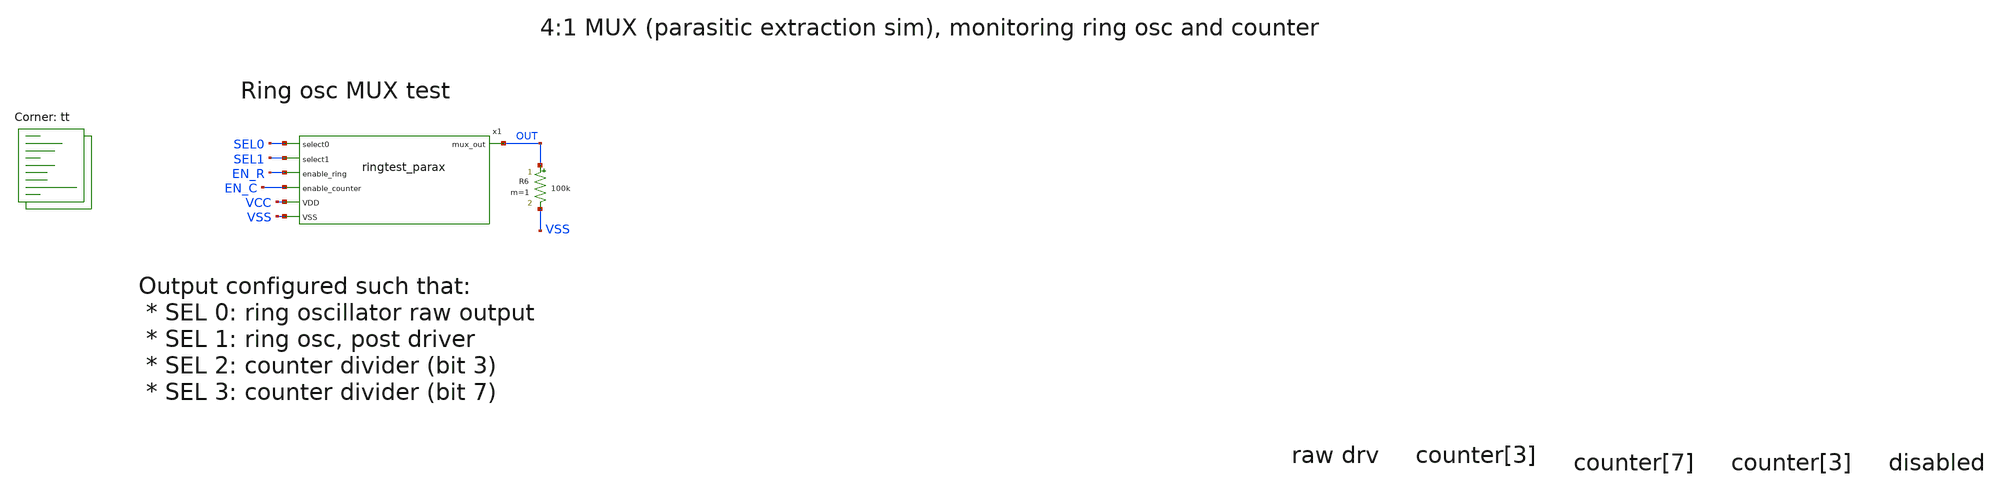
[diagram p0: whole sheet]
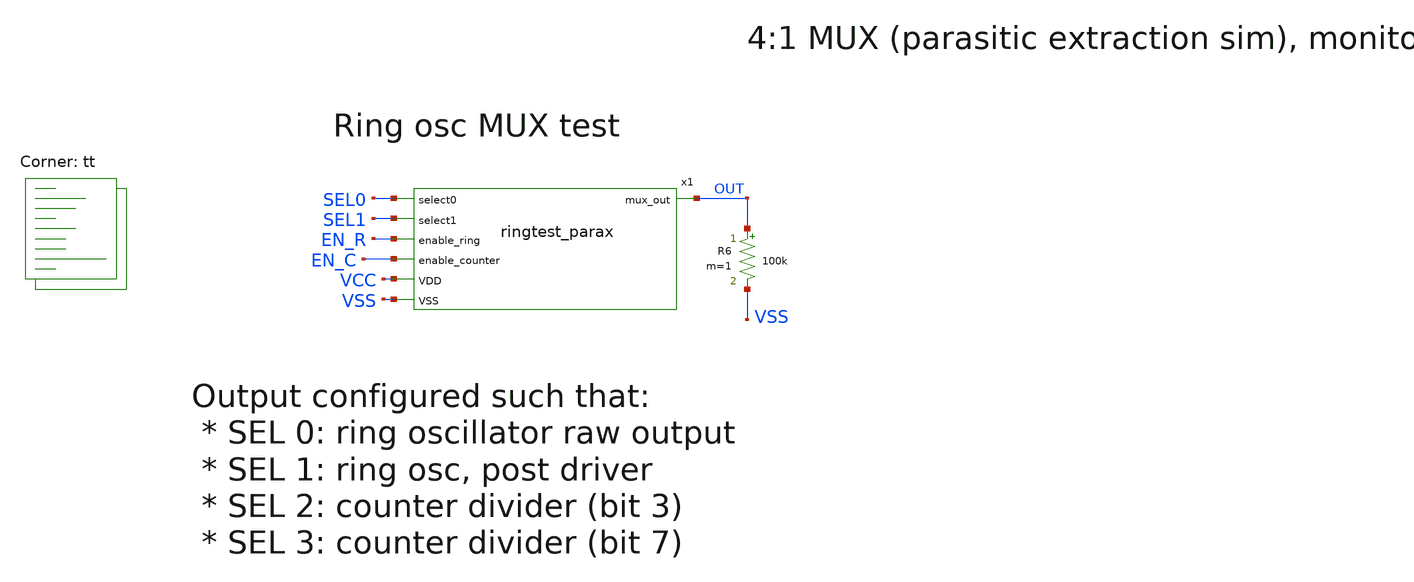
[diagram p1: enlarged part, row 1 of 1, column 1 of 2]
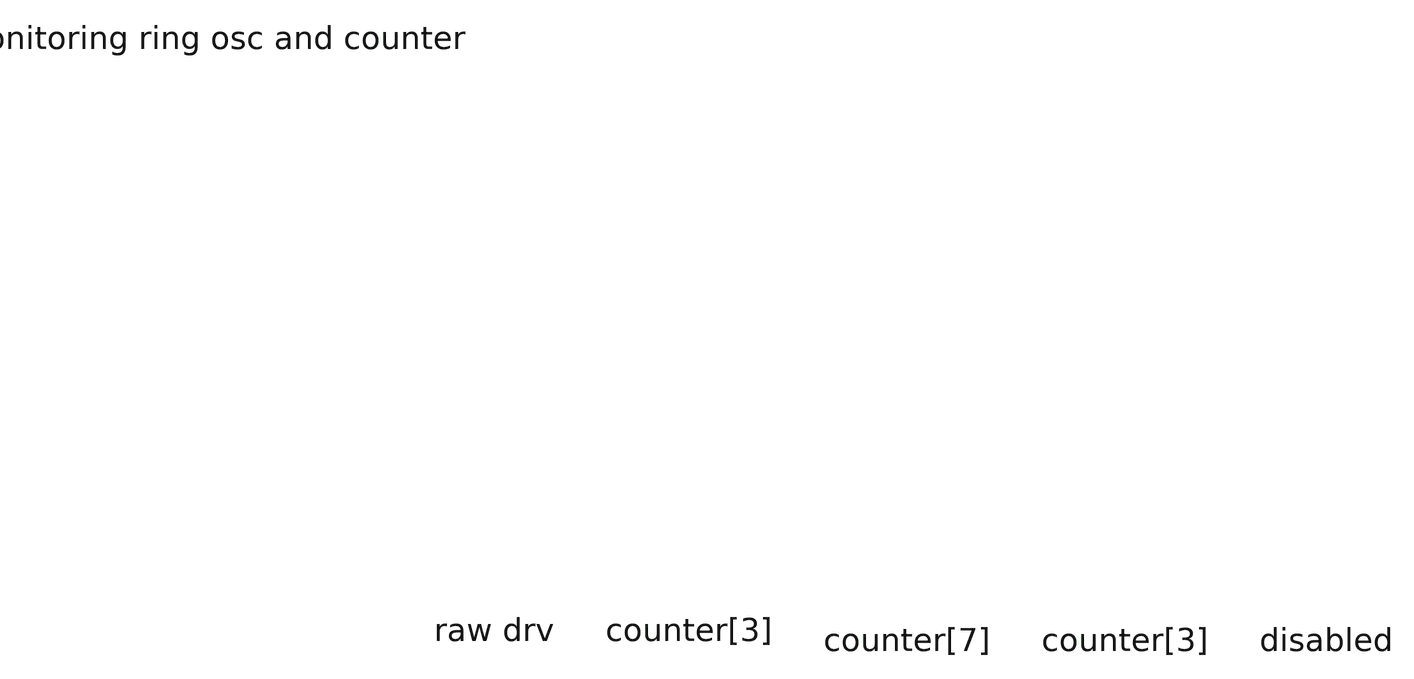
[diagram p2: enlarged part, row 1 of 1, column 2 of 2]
** sch_path: xschem/tb_ringtest.sch
**.subckt tb_ringtest
R6 OUT VSS 100k m=1
x1 VCC VSS EN_R SEL0 SEL1 EN_C OUT ringtest_parax
**** begin user architecture code
.lib $::SKYWATER_MODELS/sky130.lib.spice tt
**** end user architecture code
**.ends

* expanding   symbol:  /home/ttuser/vmswap/tt09-analogmux/xschem/ringtest_parax.sym # of pins=7
** sym_path: xschem/ringtest.sym
.include [file normalize extracted/ringtest_parax.spice]
**** begin user architecture code


* ngspice commands
* .options savecurrents
.param VCC = 1.8
.param SRCRES = 1k
.include stimuli_tb_ringtest.cir
.control
save all
op
write tb_ringtest.raw
set appendwrite
tran 0.3n 1.1u uic
write tb_ringtest.raw
quit 0
.endc



**** end user architecture code
.end
